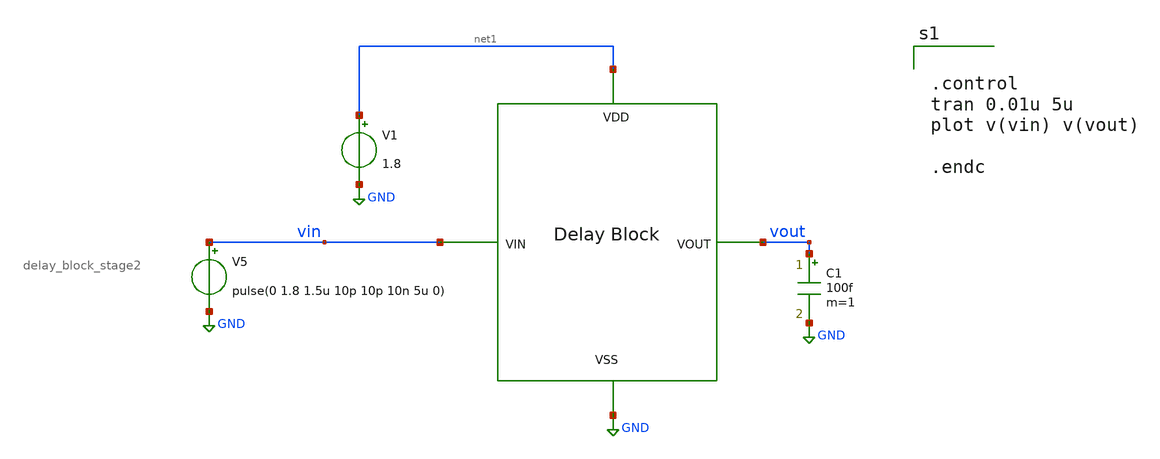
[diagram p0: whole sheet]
** sch_path: xschem/DC_DC_Converter_xschem/OTHERS/DC_DC_Converter_JV8/Delay_block_revised/Delay_block_final_tb.sch
**.subckt Delay_block_final_tb
x1 vout vin net1 GND delay_block_stage2
V1 net1 GND 1.8
V5 vin GND pulse(0 1.8 1.5u 10p 10p 10n 5u 0)
C1 vout GND 100f m=1
**** begin user architecture code


.control
tran 0.01u 5u
plot v(vin) v(vout)

.endc



** opencircuitdesign pdks install
.lib $::SKYWATER_MODELS/sky130.lib.spice tt


**** end user architecture code
**.ends
.GLOBAL GND
.end
